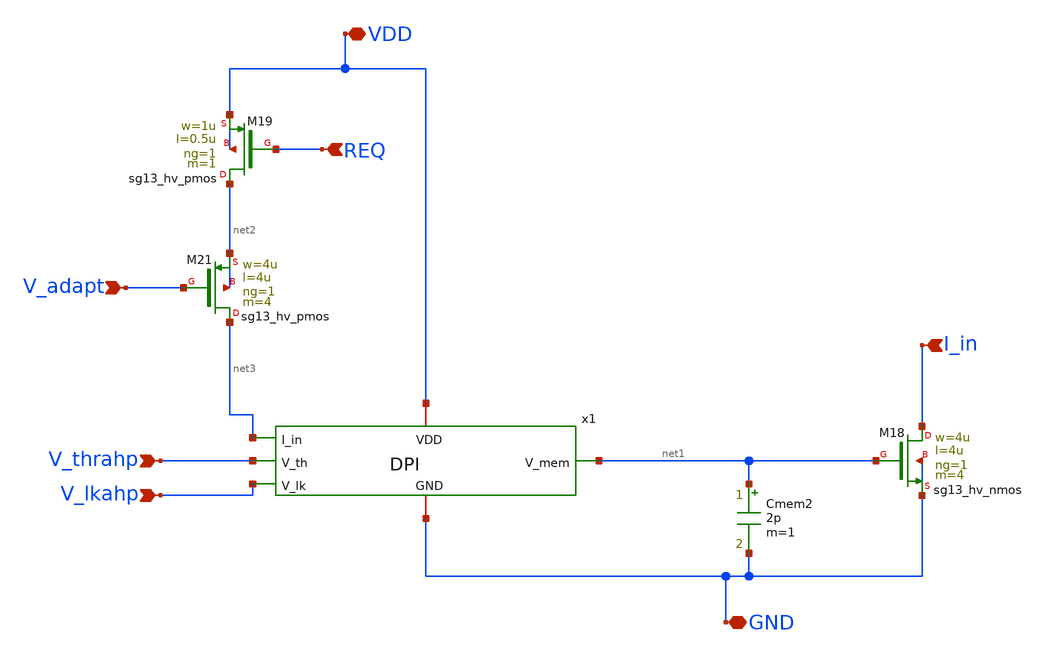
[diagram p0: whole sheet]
** sch_path: xschem/ADAP_system.sch
**.subckt ADAP_system VDD GND REQ V_adapt V_thrahp V_lkahp I_in
*.iopin VDD
*.iopin GND
*.ipin REQ
*.ipin V_adapt
*.ipin V_thrahp
*.ipin V_lkahp
*.ipin I_in
XM19 net2 REQ VDD VDD sg13_hv_pmos w=1u l=0.5u ng=1 m=1 mm_ok=1
XM21 net3 V_adapt net2 net2 sg13_hv_pmos w=4u l=4u ng=1 m=4 mm_ok=1
XM18 I_in net1 GND GND sg13_hv_nmos w=4u l=4u ng=1 m=4 mm_ok=1
Cmem2 net1 GND 2p m=1
x1 net3 VDD V_thrahp net1 V_lkahp GND DPI
**.ends

* expanding   symbol:  DPI.sym # of pins=6
** sym_path: DPI.sym
** sch_path: DPI.sch
.subckt DPI I_in VDD V_th V_mem V_lk GND
*.opin V_mem
*.ipin V_lk
*.ipin V_th
*.ipin I_in
*.iopin VDD
*.iopin GND
XM24 GND V_th I_in VDD sg13_hv_pmos w=4u l=8u ng=1 m=4 mm_ok=1
XM25 V_mem V_mem I_in VDD sg13_hv_pmos w=4u l=8u ng=1 m=4 mm_ok=1
XM28 V_mem V_lk GND GND sg13_hv_nmos w=4u l=10u ng=1 m=4 mm_ok=1
.ends

.end
